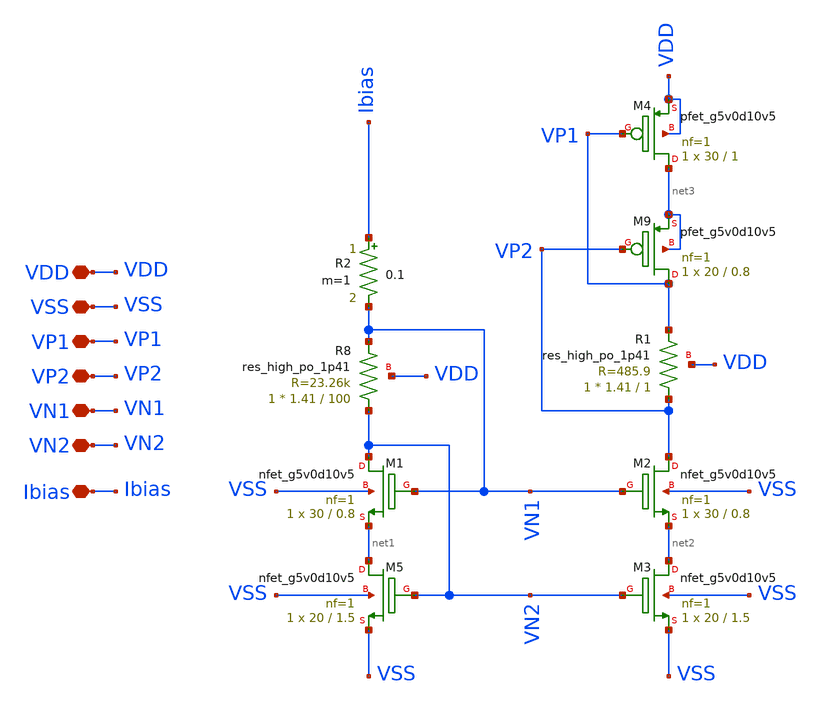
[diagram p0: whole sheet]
** sch_path: my_amp_test/second stage/vbias_gen.sch
**.subckt vbias_gen VDD VSS VP1 VP2 VN1 VN2 Ibias
*.iopin VDD
*.iopin VSS
*.iopin VP1
*.iopin VP2
*.iopin VN1
*.iopin VN2
*.iopin Ibias
XM5 net1 VN2 VSS VSS sky130_fd_pr__nfet_g5v0d10v5 L=1.5 W=20 nf=1 ad='int((1 + 1)/2) * 20 / 1 * 0.29'
+ as='int((1 + 2)/2) * 20 / 1 * 0.29' pd='2*int((1 + 1)/2) * (20 / 1 + 0.29)' ps='2*int((1 + 2)/2) * (20 / 1 + 0.29)'
+ nrd='0.29 / 20 ' nrs='0.29 / 20 ' sa=0 sb=0 sd=0 mult=1 m=1
XM1 VN2 VN1 net1 VSS sky130_fd_pr__nfet_g5v0d10v5 L=0.8 W=30 nf=1 ad='int((1 + 1)/2) * 30 / 1 * 0.29'
+ as='int((1 + 2)/2) * 30 / 1 * 0.29' pd='2*int((1 + 1)/2) * (30 / 1 + 0.29)' ps='2*int((1 + 2)/2) * (30 / 1 + 0.29)'
+ nrd='0.29 / 30 ' nrs='0.29 / 30 ' sa=0 sb=0 sd=0 mult=1 m=1
XR8 VN2 VN1 VDD sky130_fd_pr__res_high_po_1p41 L=100 mult=1 m=1
XM2 VP2 VN1 net2 VSS sky130_fd_pr__nfet_g5v0d10v5 L=0.8 W=30 nf=1 ad='int((1 + 1)/2) * 30 / 1 * 0.29'
+ as='int((1 + 2)/2) * 30 / 1 * 0.29' pd='2*int((1 + 1)/2) * (30 / 1 + 0.29)' ps='2*int((1 + 2)/2) * (30 / 1 + 0.29)'
+ nrd='0.29 / 30 ' nrs='0.29 / 30 ' sa=0 sb=0 sd=0 mult=1 m=1
XM3 net2 VN2 VSS VSS sky130_fd_pr__nfet_g5v0d10v5 L=1.5 W=20 nf=1 ad='int((1 + 1)/2) * 20 / 1 * 0.29'
+ as='int((1 + 2)/2) * 20 / 1 * 0.29' pd='2*int((1 + 1)/2) * (20 / 1 + 0.29)' ps='2*int((1 + 2)/2) * (20 / 1 + 0.29)'
+ nrd='0.29 / 20 ' nrs='0.29 / 20 ' sa=0 sb=0 sd=0 mult=1 m=1
XR1 VP2 VP1 VDD sky130_fd_pr__res_high_po_1p41 L=1 mult=1 m=1
XM9 VP1 VP2 net3 net3 sky130_fd_pr__pfet_g5v0d10v5 L=0.8 W=20 nf=1 ad='int((1 + 1)/2) * 20 / 1 * 0.29'
+ as='int((1 + 2)/2) * 20 / 1 * 0.29' pd='2*int((1 + 1)/2) * (20 / 1 + 0.29)' ps='2*int((1 + 2)/2) * (20 / 1 + 0.29)'
+ nrd='0.29 / 20 ' nrs='0.29 / 20 ' sa=0 sb=0 sd=0 mult=1 m=1
XM4 net3 VP1 VDD VDD sky130_fd_pr__pfet_g5v0d10v5 L=1 W=30 nf=1 ad='int((1 + 1)/2) * 30 / 1 * 0.29' as='int((1 + 2)/2) * 30 / 1 * 0.29'
+ pd='2*int((1 + 1)/2) * (30 / 1 + 0.29)' ps='2*int((1 + 2)/2) * (30 / 1 + 0.29)' nrd='0.29 / 30 ' nrs='0.29 / 30 '
+ sa=0 sb=0 sd=0 mult=1 m=1
R2 Ibias VN1 0.1 m=1
**.ends
.end
